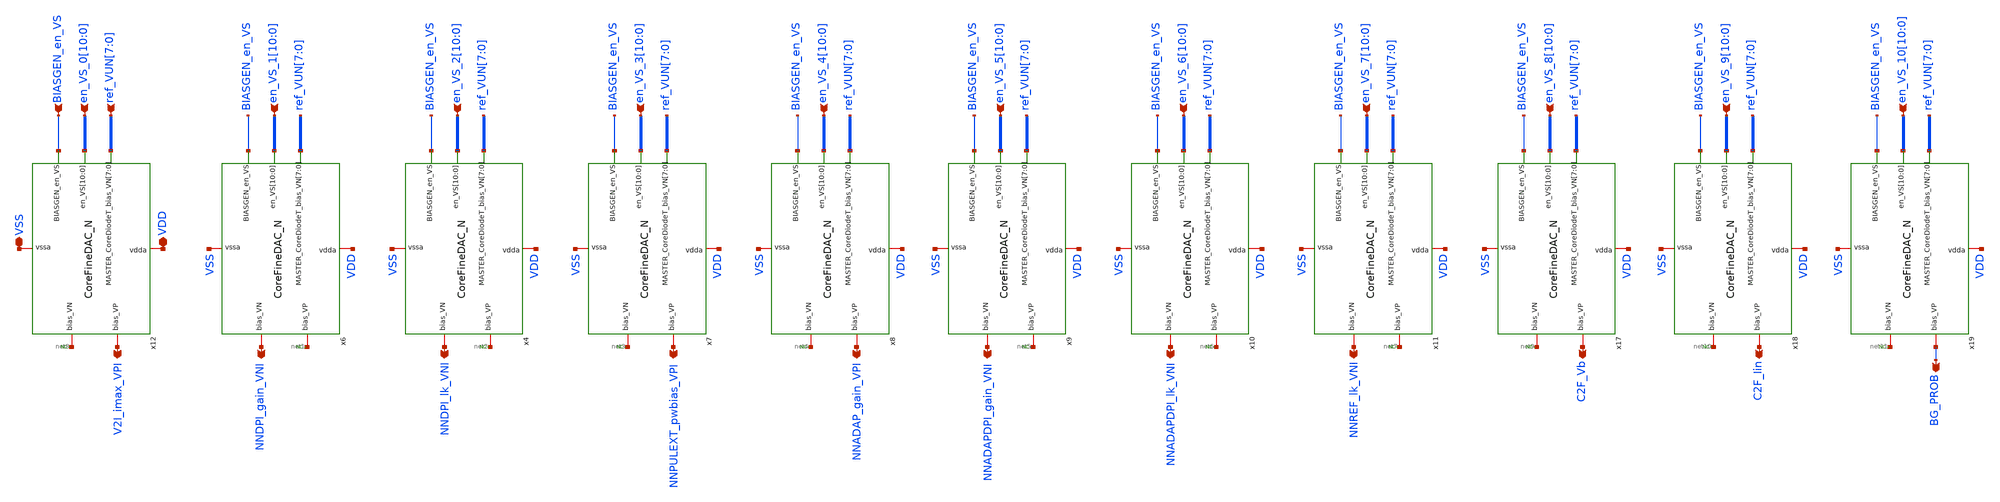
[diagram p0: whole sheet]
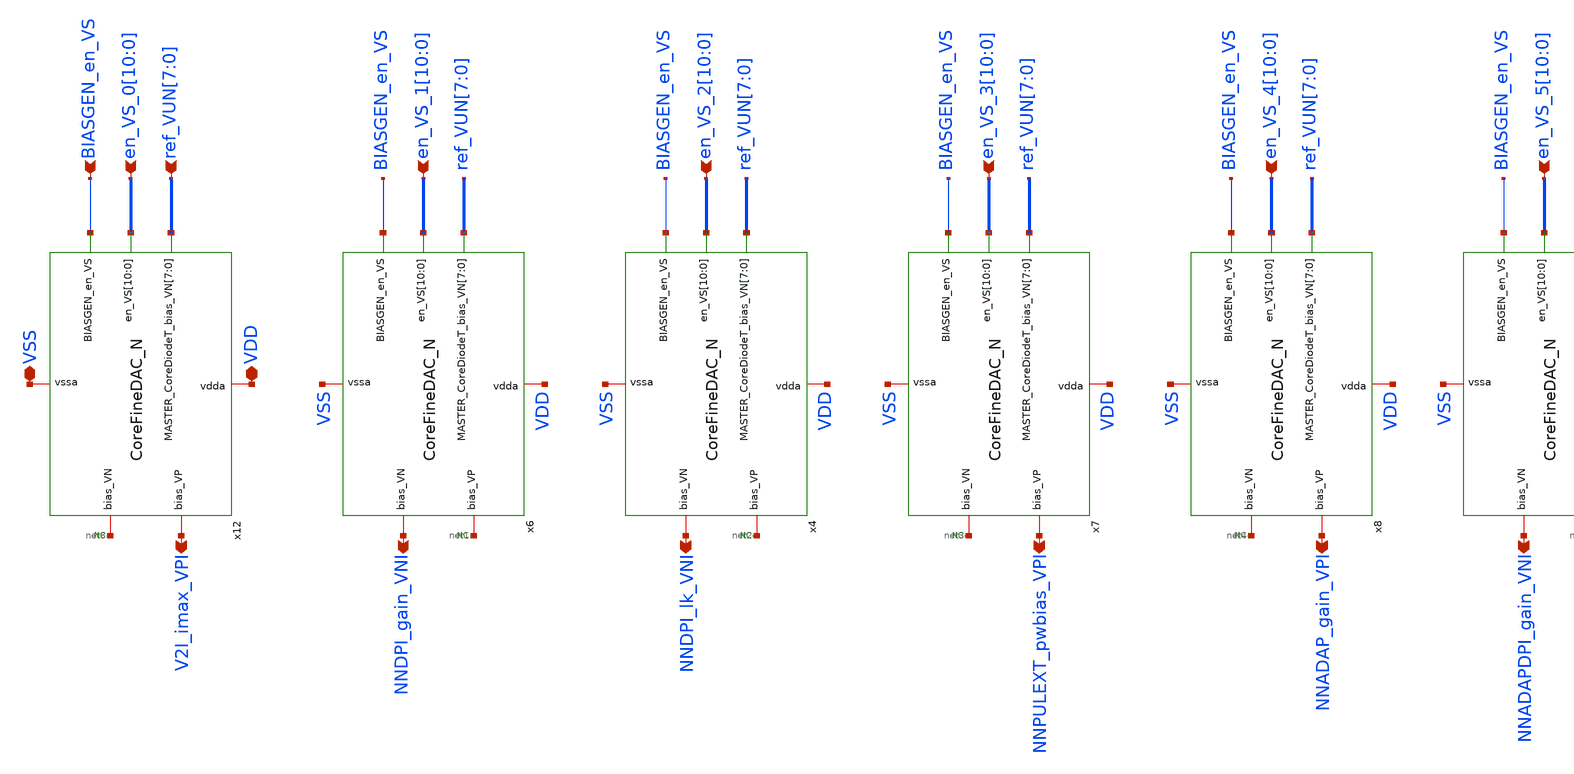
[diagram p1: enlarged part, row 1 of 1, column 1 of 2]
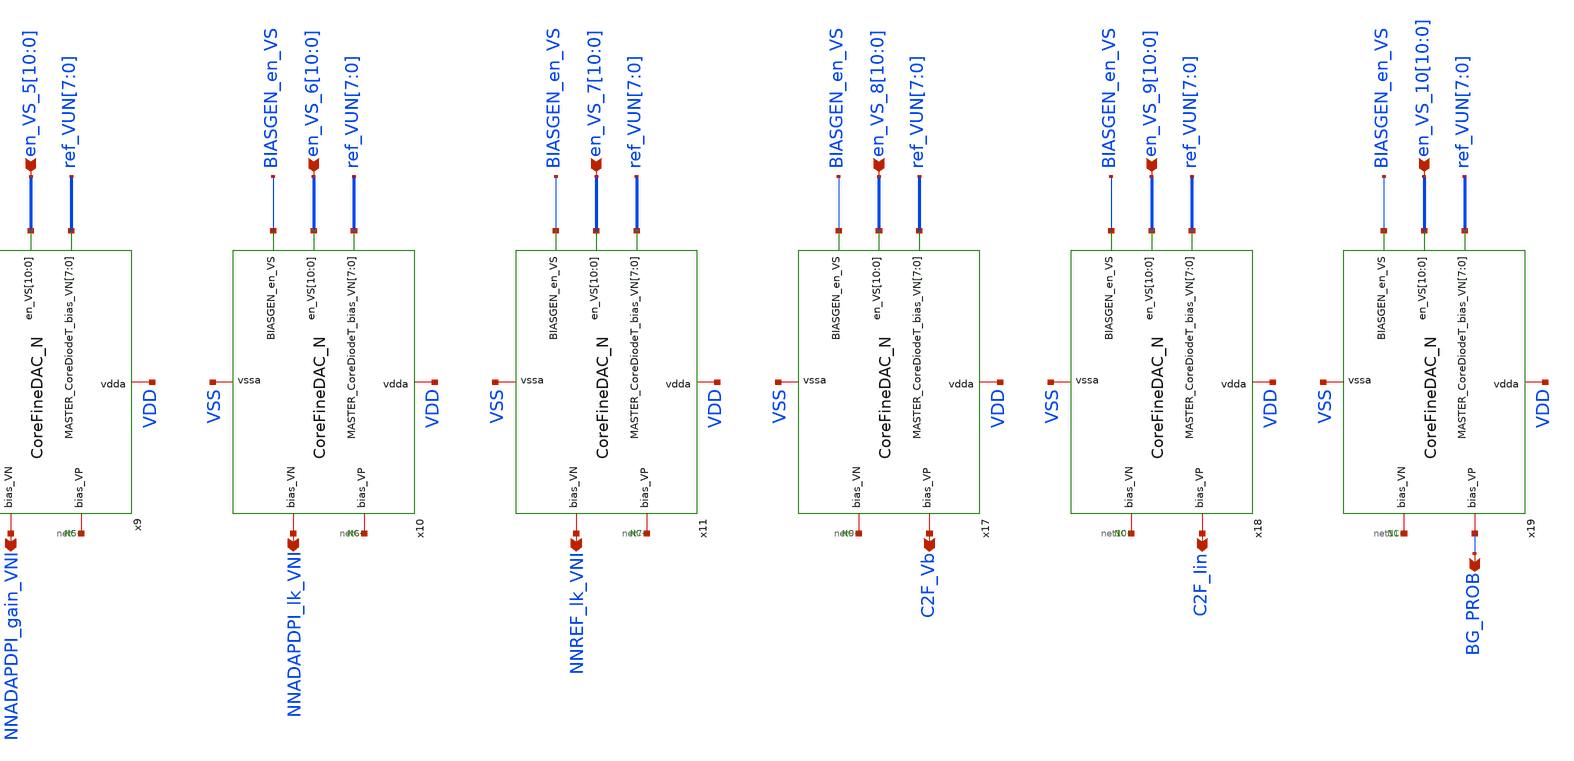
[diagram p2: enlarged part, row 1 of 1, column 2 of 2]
** sch_path: BiasBlock.sch
**.subckt BiasBlock
*+ en_VS_1[10],en_VS_1[9],en_VS_1[8],en_VS_1[7],en_VS_1[6],en_VS_1[5],en_VS_1[4],en_VS_1[3],en_VS_1[2],en_VS_1[1],en_VS_1[0] NNDPI_gain_VNI
*+ en_VS_2[10],en_VS_2[9],en_VS_2[8],en_VS_2[7],en_VS_2[6],en_VS_2[5],en_VS_2[4],en_VS_2[3],en_VS_2[2],en_VS_2[1],en_VS_2[0] NNDPI_lk_VNI
*+ en_VS_3[10],en_VS_3[9],en_VS_3[8],en_VS_3[7],en_VS_3[6],en_VS_3[5],en_VS_3[4],en_VS_3[3],en_VS_3[2],en_VS_3[1],en_VS_3[0]
*+ en_VS_4[10],en_VS_4[9],en_VS_4[8],en_VS_4[7],en_VS_4[6],en_VS_4[5],en_VS_4[4],en_VS_4[3],en_VS_4[2],en_VS_4[1],en_VS_4[0] NNPULEXT_pwbias_VPI NNADAP_gain_VPI
*+ en_VS_5[10],en_VS_5[9],en_VS_5[8],en_VS_5[7],en_VS_5[6],en_VS_5[5],en_VS_5[4],en_VS_5[3],en_VS_5[2],en_VS_5[1],en_VS_5[0]
*+ en_VS_6[10],en_VS_6[9],en_VS_6[8],en_VS_6[7],en_VS_6[6],en_VS_6[5],en_VS_6[4],en_VS_6[3],en_VS_6[2],en_VS_6[1],en_VS_6[0]
*+ en_VS_7[10],en_VS_7[9],en_VS_7[8],en_VS_7[7],en_VS_7[6],en_VS_7[5],en_VS_7[4],en_VS_7[3],en_VS_7[2],en_VS_7[1],en_VS_7[0]
*+ en_VS_0[10],en_VS_0[9],en_VS_0[8],en_VS_0[7],en_VS_0[6],en_VS_0[5],en_VS_0[4],en_VS_0[3],en_VS_0[2],en_VS_0[1],en_VS_0[0] BIASGEN_en_VS VSS VDD
*+ ref_VUN[7],ref_VUN[6],ref_VUN[5],ref_VUN[4],ref_VUN[3],ref_VUN[2],ref_VUN[1],ref_VUN[0] V2I_imax_VPI NNADAPDPI_gain_VNI NNADAPDPI_lk_VNI NNREF_lk_VNI
*+ en_VS_8[10],en_VS_8[9],en_VS_8[8],en_VS_8[7],en_VS_8[6],en_VS_8[5],en_VS_8[4],en_VS_8[3],en_VS_8[2],en_VS_8[1],en_VS_8[0]
*+ en_VS_9[10],en_VS_9[9],en_VS_9[8],en_VS_9[7],en_VS_9[6],en_VS_9[5],en_VS_9[4],en_VS_9[3],en_VS_9[2],en_VS_9[1],en_VS_9[0]
*+ en_VS_10[10],en_VS_10[9],en_VS_10[8],en_VS_10[7],en_VS_10[6],en_VS_10[5],en_VS_10[4],en_VS_10[3],en_VS_10[2],en_VS_10[1],en_VS_10[0] BG_PROB C2F_Iin C2F_Vb
*.ipin
*+ en_VS_1[10],en_VS_1[9],en_VS_1[8],en_VS_1[7],en_VS_1[6],en_VS_1[5],en_VS_1[4],en_VS_1[3],en_VS_1[2],en_VS_1[1],en_VS_1[0]
*.opin NNDPI_gain_VNI
*.ipin
*+ en_VS_2[10],en_VS_2[9],en_VS_2[8],en_VS_2[7],en_VS_2[6],en_VS_2[5],en_VS_2[4],en_VS_2[3],en_VS_2[2],en_VS_2[1],en_VS_2[0]
*.opin NNDPI_lk_VNI
*.ipin
*+ en_VS_3[10],en_VS_3[9],en_VS_3[8],en_VS_3[7],en_VS_3[6],en_VS_3[5],en_VS_3[4],en_VS_3[3],en_VS_3[2],en_VS_3[1],en_VS_3[0]
*.ipin
*+ en_VS_4[10],en_VS_4[9],en_VS_4[8],en_VS_4[7],en_VS_4[6],en_VS_4[5],en_VS_4[4],en_VS_4[3],en_VS_4[2],en_VS_4[1],en_VS_4[0]
*.opin NNPULEXT_pwbias_VPI
*.opin NNADAP_gain_VPI
*.ipin
*+ en_VS_5[10],en_VS_5[9],en_VS_5[8],en_VS_5[7],en_VS_5[6],en_VS_5[5],en_VS_5[4],en_VS_5[3],en_VS_5[2],en_VS_5[1],en_VS_5[0]
*.ipin
*+ en_VS_6[10],en_VS_6[9],en_VS_6[8],en_VS_6[7],en_VS_6[6],en_VS_6[5],en_VS_6[4],en_VS_6[3],en_VS_6[2],en_VS_6[1],en_VS_6[0]
*.ipin
*+ en_VS_7[10],en_VS_7[9],en_VS_7[8],en_VS_7[7],en_VS_7[6],en_VS_7[5],en_VS_7[4],en_VS_7[3],en_VS_7[2],en_VS_7[1],en_VS_7[0]
*.ipin
*+ en_VS_0[10],en_VS_0[9],en_VS_0[8],en_VS_0[7],en_VS_0[6],en_VS_0[5],en_VS_0[4],en_VS_0[3],en_VS_0[2],en_VS_0[1],en_VS_0[0]
*.ipin BIASGEN_en_VS
*.iopin VSS
*.iopin VDD
*.ipin ref_VUN[7],ref_VUN[6],ref_VUN[5],ref_VUN[4],ref_VUN[3],ref_VUN[2],ref_VUN[1],ref_VUN[0]
*.opin V2I_imax_VPI
*.opin NNADAPDPI_gain_VNI
*.opin NNADAPDPI_lk_VNI
*.opin NNREF_lk_VNI
*.ipin
*+ en_VS_8[10],en_VS_8[9],en_VS_8[8],en_VS_8[7],en_VS_8[6],en_VS_8[5],en_VS_8[4],en_VS_8[3],en_VS_8[2],en_VS_8[1],en_VS_8[0]
*.ipin
*+ en_VS_9[10],en_VS_9[9],en_VS_9[8],en_VS_9[7],en_VS_9[6],en_VS_9[5],en_VS_9[4],en_VS_9[3],en_VS_9[2],en_VS_9[1],en_VS_9[0]
*.ipin
*+ en_VS_10[10],en_VS_10[9],en_VS_10[8],en_VS_10[7],en_VS_10[6],en_VS_10[5],en_VS_10[4],en_VS_10[3],en_VS_10[2],en_VS_10[1],en_VS_10[0]
*.opin BG_PROB
*.opin C2F_Iin
*.opin C2F_Vb
x6 en_VS_1[10] en_VS_1[9] en_VS_1[8] en_VS_1[7] en_VS_1[6] en_VS_1[5] en_VS_1[4] en_VS_1[3]
+ en_VS_1[2] en_VS_1[1] en_VS_1[0] VSS VDD net1 NNDPI_gain_VNI ref_VUN[7] ref_VUN[6] ref_VUN[5] ref_VUN[4]
+ ref_VUN[3] ref_VUN[2] ref_VUN[1] ref_VUN[0] BIASGEN_en_VS CoreFineDAC_N
x4 en_VS_2[10] en_VS_2[9] en_VS_2[8] en_VS_2[7] en_VS_2[6] en_VS_2[5] en_VS_2[4] en_VS_2[3]
+ en_VS_2[2] en_VS_2[1] en_VS_2[0] VSS VDD net2 NNDPI_lk_VNI ref_VUN[7] ref_VUN[6] ref_VUN[5] ref_VUN[4]
+ ref_VUN[3] ref_VUN[2] ref_VUN[1] ref_VUN[0] BIASGEN_en_VS CoreFineDAC_N
x7 en_VS_3[10] en_VS_3[9] en_VS_3[8] en_VS_3[7] en_VS_3[6] en_VS_3[5] en_VS_3[4] en_VS_3[3]
+ en_VS_3[2] en_VS_3[1] en_VS_3[0] VSS VDD NNPULEXT_pwbias_VPI net3 ref_VUN[7] ref_VUN[6] ref_VUN[5] ref_VUN[4]
+ ref_VUN[3] ref_VUN[2] ref_VUN[1] ref_VUN[0] BIASGEN_en_VS CoreFineDAC_N
x8 en_VS_4[10] en_VS_4[9] en_VS_4[8] en_VS_4[7] en_VS_4[6] en_VS_4[5] en_VS_4[4] en_VS_4[3]
+ en_VS_4[2] en_VS_4[1] en_VS_4[0] VSS VDD NNADAP_gain_VPI net4 ref_VUN[7] ref_VUN[6] ref_VUN[5] ref_VUN[4]
+ ref_VUN[3] ref_VUN[2] ref_VUN[1] ref_VUN[0] BIASGEN_en_VS CoreFineDAC_N
x9 en_VS_5[10] en_VS_5[9] en_VS_5[8] en_VS_5[7] en_VS_5[6] en_VS_5[5] en_VS_5[4] en_VS_5[3]
+ en_VS_5[2] en_VS_5[1] en_VS_5[0] VSS VDD net5 NNADAPDPI_gain_VNI ref_VUN[7] ref_VUN[6] ref_VUN[5] ref_VUN[4]
+ ref_VUN[3] ref_VUN[2] ref_VUN[1] ref_VUN[0] BIASGEN_en_VS CoreFineDAC_N
x10 en_VS_6[10] en_VS_6[9] en_VS_6[8] en_VS_6[7] en_VS_6[6] en_VS_6[5] en_VS_6[4] en_VS_6[3]
+ en_VS_6[2] en_VS_6[1] en_VS_6[0] VSS VDD net6 NNADAPDPI_lk_VNI ref_VUN[7] ref_VUN[6] ref_VUN[5] ref_VUN[4]
+ ref_VUN[3] ref_VUN[2] ref_VUN[1] ref_VUN[0] BIASGEN_en_VS CoreFineDAC_N
x11 en_VS_7[10] en_VS_7[9] en_VS_7[8] en_VS_7[7] en_VS_7[6] en_VS_7[5] en_VS_7[4] en_VS_7[3]
+ en_VS_7[2] en_VS_7[1] en_VS_7[0] VSS VDD net7 NNREF_lk_VNI ref_VUN[7] ref_VUN[6] ref_VUN[5] ref_VUN[4]
+ ref_VUN[3] ref_VUN[2] ref_VUN[1] ref_VUN[0] BIASGEN_en_VS CoreFineDAC_N
x12 en_VS_0[10] en_VS_0[9] en_VS_0[8] en_VS_0[7] en_VS_0[6] en_VS_0[5] en_VS_0[4] en_VS_0[3]
+ en_VS_0[2] en_VS_0[1] en_VS_0[0] VSS VDD V2I_imax_VPI net8 ref_VUN[7] ref_VUN[6] ref_VUN[5] ref_VUN[4]
+ ref_VUN[3] ref_VUN[2] ref_VUN[1] ref_VUN[0] BIASGEN_en_VS CoreFineDAC_N
x17 en_VS_8[10] en_VS_8[9] en_VS_8[8] en_VS_8[7] en_VS_8[6] en_VS_8[5] en_VS_8[4] en_VS_8[3]
+ en_VS_8[2] en_VS_8[1] en_VS_8[0] VSS VDD C2F_Vb net9 ref_VUN[7] ref_VUN[6] ref_VUN[5] ref_VUN[4] ref_VUN[3]
+ ref_VUN[2] ref_VUN[1] ref_VUN[0] BIASGEN_en_VS CoreFineDAC_N
x18 en_VS_9[10] en_VS_9[9] en_VS_9[8] en_VS_9[7] en_VS_9[6] en_VS_9[5] en_VS_9[4] en_VS_9[3]
+ en_VS_9[2] en_VS_9[1] en_VS_9[0] VSS VDD C2F_Iin net10 ref_VUN[7] ref_VUN[6] ref_VUN[5] ref_VUN[4] ref_VUN[3]
+ ref_VUN[2] ref_VUN[1] ref_VUN[0] BIASGEN_en_VS CoreFineDAC_N
x19 en_VS_10[10] en_VS_10[9] en_VS_10[8] en_VS_10[7] en_VS_10[6] en_VS_10[5] en_VS_10[4] en_VS_10[3]
+ en_VS_10[2] en_VS_10[1] en_VS_10[0] VSS VDD BG_PROB net11 ref_VUN[7] ref_VUN[6] ref_VUN[5] ref_VUN[4]
+ ref_VUN[3] ref_VUN[2] ref_VUN[1] ref_VUN[0] BIASGEN_en_VS CoreFineDAC_N
* noconn #net8
* noconn #net1
* noconn #net2
* noconn #net3
* noconn #net4
* noconn #net5
* noconn #net6
* noconn #net7
* noconn #net9
* noconn #net10
* noconn #net11
**.ends
.end
